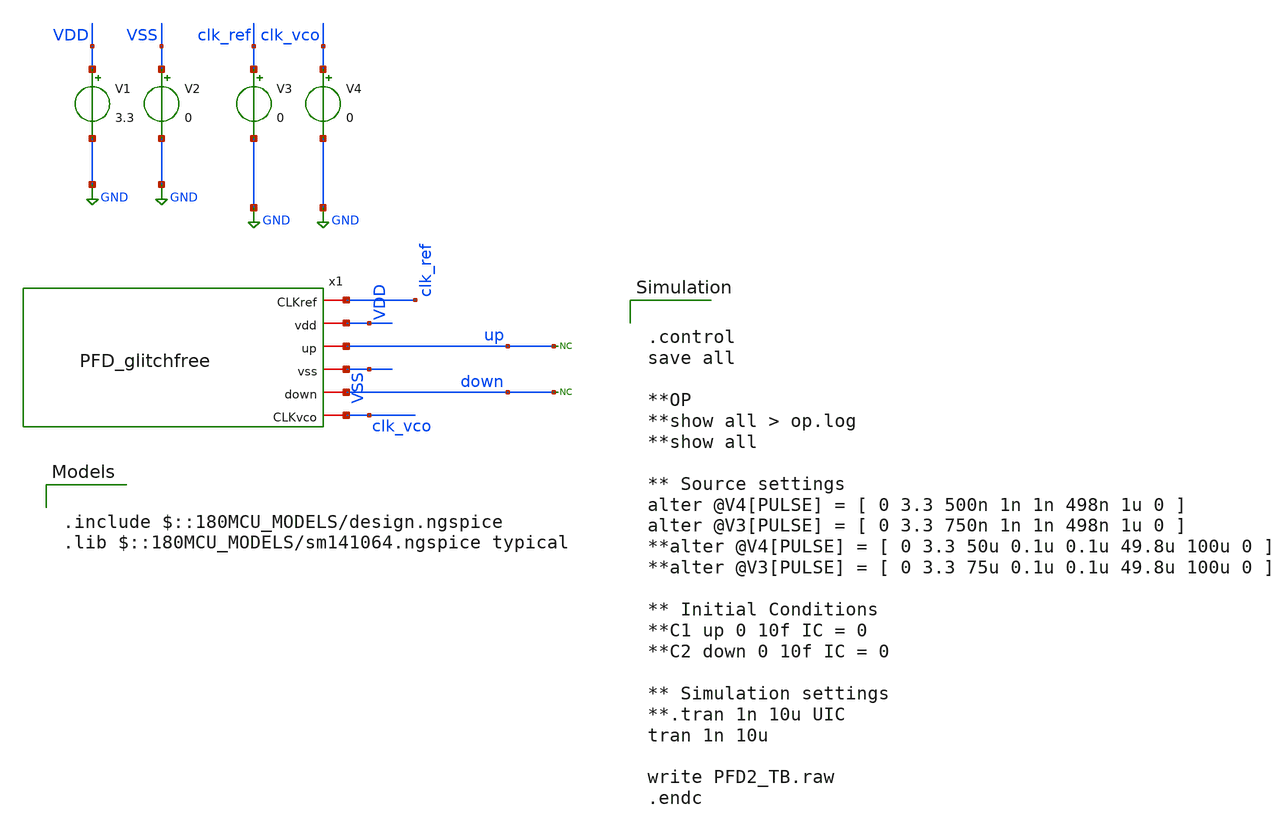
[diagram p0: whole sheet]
** sch_path: designs/libs/qw_core_analog/PFDglitchfree_TB.sch
**.subckt PFDglitchfree_TB
V1 VDD GND 3.3
V2 VSS GND 0
* noconn up
* noconn down
V3 clk_ref GND 0
V4 clk_vco GND 0
x1 clk_ref VDD up VSS down clk_vco PFD_glitchfree
**** begin user architecture code

.include $::180MCU_MODELS/design.ngspice
.lib $::180MCU_MODELS/sm141064.ngspice typical



.control
save all

**OP
**show all > op.log
**show all

** Source settings
alter @V4[PULSE] = [ 0 3.3 500n 1n 1n 498n 1u 0 ]
alter @V3[PULSE] = [ 0 3.3 750n 1n 1n 498n 1u 0 ]
**alter @V4[PULSE] = [ 0 3.3 50u 0.1u 0.1u 49.8u 100u 0 ]
**alter @V3[PULSE] = [ 0 3.3 75u 0.1u 0.1u 49.8u 100u 0 ]

** Initial Conditions
**C1 up 0 10f IC = 0
**C2 down 0 10f IC = 0

** Simulation settings
**.tran 1n 10u UIC
tran 1n 10u

write PFD2_TB.raw
.endc


**** end user architecture code
**.ends

* expanding   symbol:  PFD_glitchfree.sym # of pins=6
** sym_path: designs/libs/xp_core_analog/PFD_new/PFD_glitchfree.sym
** sch_path: designs/libs/xp_core_analog/PFD_new/PFD_glitchfree.sch
.subckt PFD_glitchfree CLKref vdd up vss down CLKvco
*.iopin CLKref
*.iopin CLKvco
*.iopin vdd
*.iopin vss
*.iopin up
*.iopin down
XM1 net1 CLKref net5 vss nfet_03v3 L=0.28u W=1u nf=1 ad='int((nf+1)/2) * W/nf * 0.18u' as='int((nf+2)/2) * W/nf * 0.18u'
+ pd='2*int((nf+1)/2) * (W/nf + 0.18u)' ps='2*int((nf+2)/2) * (W/nf + 0.18u)' nrd='0.18u / W' nrs='0.18u / W'
+ sa=0 sb=0 sd=0 m=1
XM2 net1 CLKref vdd vdd pfet_03v3 L=0.28u W=1u nf=1 ad='int((nf+1)/2) * W/nf * 0.18u' as='int((nf+2)/2) * W/nf * 0.18u'
+ pd='2*int((nf+1)/2) * (W/nf + 0.18u)' ps='2*int((nf+2)/2) * (W/nf + 0.18u)' nrd='0.18u / W' nrs='0.18u / W'
+ sa=0 sb=0 sd=0 m=1
XM3 net1 down net2 vss nfet_03v3 L=0.28u W=1u nf=1 ad='int((nf+1)/2) * W/nf * 0.18u' as='int((nf+2)/2) * W/nf * 0.18u'
+ pd='2*int((nf+1)/2) * (W/nf + 0.18u)' ps='2*int((nf+2)/2) * (W/nf + 0.18u)' nrd='0.18u / W' nrs='0.18u / W'
+ sa=0 sb=0 sd=0 m=1
XM4 net1 CLKvco net2 vss nfet_03v3 L=0.28u W=1u nf=1 ad='int((nf+1)/2) * W/nf * 0.18u' as='int((nf+2)/2) * W/nf * 0.18u'
+ pd='2*int((nf+1)/2) * (W/nf + 0.18u)' ps='2*int((nf+2)/2) * (W/nf + 0.18u)' nrd='0.18u / W' nrs='0.18u / W'
+ sa=0 sb=0 sd=0 m=1
XM5 net2 CLKref vss vss nfet_03v3 L=0.28u W=1u nf=1 ad='int((nf+1)/2) * W/nf * 0.18u' as='int((nf+2)/2) * W/nf * 0.18u'
+ pd='2*int((nf+1)/2) * (W/nf + 0.18u)' ps='2*int((nf+2)/2) * (W/nf + 0.18u)' nrd='0.18u / W' nrs='0.18u / W'
+ sa=0 sb=0 sd=0 m=1
XM6 net3 CLKvco net7 vss nfet_03v3 L=0.28u W=1u nf=1 ad='int((nf+1)/2) * W/nf * 0.18u' as='int((nf+2)/2) * W/nf * 0.18u'
+ pd='2*int((nf+1)/2) * (W/nf + 0.18u)' ps='2*int((nf+2)/2) * (W/nf + 0.18u)' nrd='0.18u / W' nrs='0.18u / W'
+ sa=0 sb=0 sd=0 m=1
XM7 net3 CLKvco vdd vdd pfet_03v3 L=0.28u W=1u nf=1 ad='int((nf+1)/2) * W/nf * 0.18u' as='int((nf+2)/2) * W/nf * 0.18u'
+ pd='2*int((nf+1)/2) * (W/nf + 0.18u)' ps='2*int((nf+2)/2) * (W/nf + 0.18u)' nrd='0.18u / W' nrs='0.18u / W'
+ sa=0 sb=0 sd=0 m=1
XM8 net3 up net4 vss nfet_03v3 L=0.28u W=1u nf=1 ad='int((nf+1)/2) * W/nf * 0.18u' as='int((nf+2)/2) * W/nf * 0.18u'
+ pd='2*int((nf+1)/2) * (W/nf + 0.18u)' ps='2*int((nf+2)/2) * (W/nf + 0.18u)' nrd='0.18u / W' nrs='0.18u / W'
+ sa=0 sb=0 sd=0 m=1
XM9 net3 CLKref net4 vss nfet_03v3 L=0.28u W=1u nf=1 ad='int((nf+1)/2) * W/nf * 0.18u' as='int((nf+2)/2) * W/nf * 0.18u'
+ pd='2*int((nf+1)/2) * (W/nf + 0.18u)' ps='2*int((nf+2)/2) * (W/nf + 0.18u)' nrd='0.18u / W' nrs='0.18u / W'
+ sa=0 sb=0 sd=0 m=1
XM10 net4 CLKvco vss vss nfet_03v3 L=0.28u W=1u nf=1 ad='int((nf+1)/2) * W/nf * 0.18u' as='int((nf+2)/2) * W/nf * 0.18u'
+ pd='2*int((nf+1)/2) * (W/nf + 0.18u)' ps='2*int((nf+2)/2) * (W/nf + 0.18u)' nrd='0.18u / W' nrs='0.18u / W'
+ sa=0 sb=0 sd=0 m=1
XM11 net6 net5 vdd vdd pfet_03v3 L=0.28u W=1u nf=1 ad='int((nf+1)/2) * W/nf * 0.18u' as='int((nf+2)/2) * W/nf * 0.18u'
+ pd='2*int((nf+1)/2) * (W/nf + 0.18u)' ps='2*int((nf+2)/2) * (W/nf + 0.18u)' nrd='0.18u / W' nrs='0.18u / W'
+ sa=0 sb=0 sd=0 m=1
XM12 net6 net5 vss vss nfet_03v3 L=0.28u W=0.5u nf=1 ad='int((nf+1)/2) * W/nf * 0.18u' as='int((nf+2)/2) * W/nf * 0.18u'
+ pd='2*int((nf+1)/2) * (W/nf + 0.18u)' ps='2*int((nf+2)/2) * (W/nf + 0.18u)' nrd='0.18u / W' nrs='0.18u / W'
+ sa=0 sb=0 sd=0 m=1
XM13 up net6 vdd vdd pfet_03v3 L=0.28u W=1u nf=1 ad='int((nf+1)/2) * W/nf * 0.18u' as='int((nf+2)/2) * W/nf * 0.18u'
+ pd='2*int((nf+1)/2) * (W/nf + 0.18u)' ps='2*int((nf+2)/2) * (W/nf + 0.18u)' nrd='0.18u / W' nrs='0.18u / W'
+ sa=0 sb=0 sd=0 m=1
XM14 up net6 vss vss nfet_03v3 L=0.28u W=0.5u nf=1 ad='int((nf+1)/2) * W/nf * 0.18u' as='int((nf+2)/2) * W/nf * 0.18u'
+ pd='2*int((nf+1)/2) * (W/nf + 0.18u)' ps='2*int((nf+2)/2) * (W/nf + 0.18u)' nrd='0.18u / W' nrs='0.18u / W'
+ sa=0 sb=0 sd=0 m=1
XM15 net8 net7 vdd vdd pfet_03v3 L=0.28u W=1u nf=1 ad='int((nf+1)/2) * W/nf * 0.18u' as='int((nf+2)/2) * W/nf * 0.18u'
+ pd='2*int((nf+1)/2) * (W/nf + 0.18u)' ps='2*int((nf+2)/2) * (W/nf + 0.18u)' nrd='0.18u / W' nrs='0.18u / W'
+ sa=0 sb=0 sd=0 m=1
XM16 net8 net7 vss vss nfet_03v3 L=0.28u W=0.5u nf=1 ad='int((nf+1)/2) * W/nf * 0.18u' as='int((nf+2)/2) * W/nf * 0.18u'
+ pd='2*int((nf+1)/2) * (W/nf + 0.18u)' ps='2*int((nf+2)/2) * (W/nf + 0.18u)' nrd='0.18u / W' nrs='0.18u / W'
+ sa=0 sb=0 sd=0 m=1
XM17 down net8 vdd vdd pfet_03v3 L=0.28u W=1u nf=1 ad='int((nf+1)/2) * W/nf * 0.18u' as='int((nf+2)/2) * W/nf * 0.18u'
+ pd='2*int((nf+1)/2) * (W/nf + 0.18u)' ps='2*int((nf+2)/2) * (W/nf + 0.18u)' nrd='0.18u / W' nrs='0.18u / W'
+ sa=0 sb=0 sd=0 m=1
XM18 down net8 vss vss nfet_03v3 L=0.28u W=0.5u nf=1 ad='int((nf+1)/2) * W/nf * 0.18u' as='int((nf+2)/2) * W/nf * 0.18u'
+ pd='2*int((nf+1)/2) * (W/nf + 0.18u)' ps='2*int((nf+2)/2) * (W/nf + 0.18u)' nrd='0.18u / W' nrs='0.18u / W'
+ sa=0 sb=0 sd=0 m=1
.ends

.GLOBAL GND
.end
